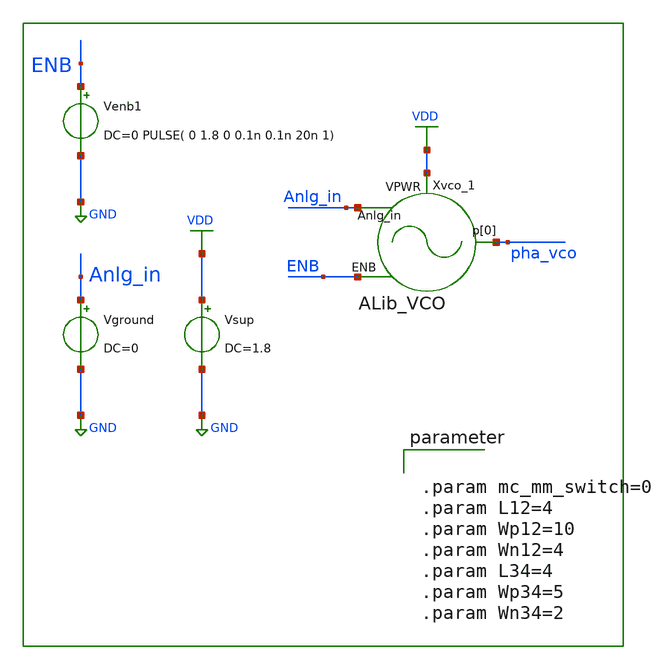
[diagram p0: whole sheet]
** sch_path: xschem/tb/VCO_tb.sch
**.subckt VCO_tb
Vsup VDD GND DC=1.8
Vground Anlg_in GND DC=0
Venb1 ENB GND DC=0 PULSE( 0 1.8 0 0.1n 0.1n 20n 1)
Xvco_1 VDD pha_vco Anlg_in ENB ALib_VCO L12="L12" Wp12="Wp12" Wn12="Wn12" L34="L34" Wp34="Wp34"
+ Wn34="Wn34"
**** begin user architecture code


.control
set nobreak
set num_threads=4
set test_mode = 0
* mode = 0: operation testing				1:  frequency extraction    2:  power consumption
if ($test_mode = 0)
    TRAN 1n 5u
    plot pha_vco
    MEAS TRAN prd TRIG pha_vco VAL=0.8 RISE=10 TARG pha_vco VAL=0.8 RISE=20
    let freq = 10/prd
    echo "frequency: "
    print freq
end
if ($test_mode = 1)
    let Vlow = 0
    let Vlimit = 1.01     $ set upper bound for sweeping
    let Vsweep = 0.2      $ set step size for sweeping
    let NoPoints=(Vlimit-Vlow)/Vsweep+2    $ set number of points for sweeping
    let freq =unitvec(NoPoints)
    let Vin  =unitvec(NoPoints)
    let Vin[0]=Vlow
    let ix=0
    while Vin[ix] < Vlimit
        alter Vground DC=Vin[ix]
        TRAN 0.4n 12u
        MEAS TRAN prd TRIG pha_vco VAL=0.8 RISE=10 TARG pha_vco VAL=0.8 RISE =20
        let freq[ix] = 10/prd
        let ix = ix+1
        Let Vin[ix] = Vin[ix-1]+Vsweep
    end
   print Vin freq
end
if ($test_mode = 2)
    save "vdd" @Vsup[i] "p[0]"
    TRAN 0.1n 5u
    MEAS TRAN I_vco AVG @Vsup[i] FROM=3u TO=4u
    MEAS TRAN V_vco AVG vdd FROM=3u TO=4u
    let Power=I_vco*V_vco
    print Power
end
.endc




** Library on VNU server
.lib /home/dkits/efabless/mpw-5/pdks/sky130A/libs.tech/ngspice/sky130.lib.spice tt
.inc /home/dkits/efabless/mpw-5/pdks/sky130A/libs.ref/sky130_fd_sc_hd/spice/sky130_fd_sc_hd.spice
** Library on Home PC
*.lib /home/dkit/efabless/pdks/sky130A/libs.tech/ngspice/sky130.lib.spice tt
*.inc /home/dkit/efabless/pdks/sky130A/libs.ref/sky130_fd_sc_hd/spice/sky130_fd_sc_hd.spice




.param mc_mm_switch=0
.param L12=4
.param Wp12=10
.param Wn12=4
.param L34=4
.param Wp34=5
.param Wn34=2


**** end user architecture code
**.ends
.GLOBAL VDD
.GLOBAL GND
.end
